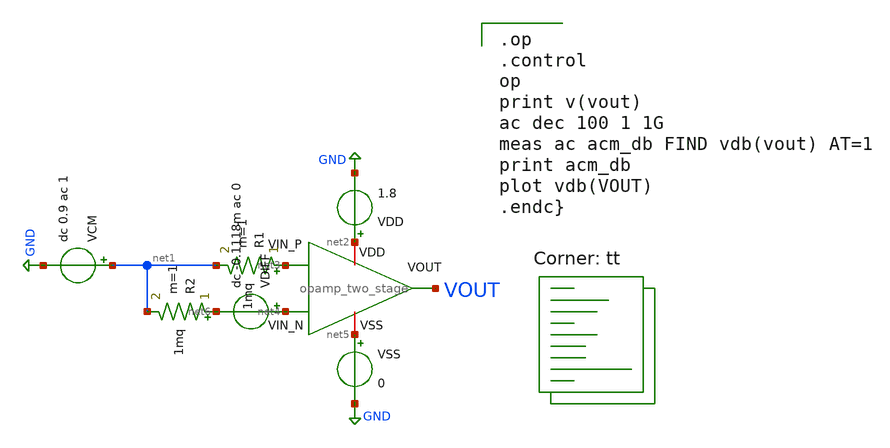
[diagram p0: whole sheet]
** sch_path: analog/bootcamp_opamp/schematics/tb_cmrr.sch
**.subckt tb_cmrr
x1 net2 VOUT net3 net4 net5 opamp_two_stage
VSS net5 GND 0
VDD net2 GND 1.8
VCM net1 GND dc 0.9 ac 1
VDIFF net4 net6 dc -0.1118m ac 0
R1 net3 net1 1mq m=1
R2 net6 net1 1mq m=1
**** begin user architecture code

.op
.control
op
print v(vout)
ac dec 100 1 1G
meas ac acm_db FIND vdb(vout) AT=1
print acm_db
plot vdb(VOUT)
.endc}

.lib $::SKYWATER_MODELS/sky130.lib.spice tt
**** end user architecture code
**.ends
.GLOBAL GND
.end
